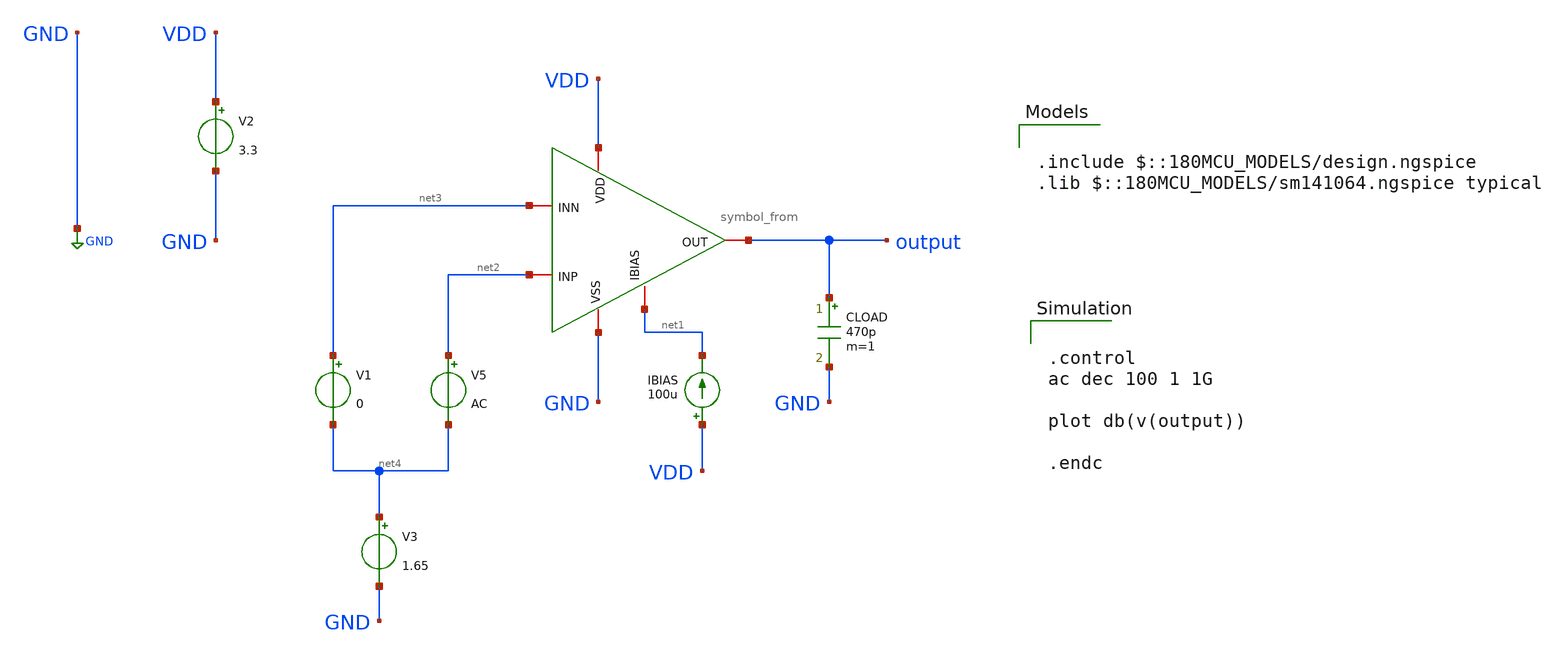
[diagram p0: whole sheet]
** sch_path: designs/libs/core_amps/ota_folded_cascode/folded_cascode_tb.sch
**.subckt folded_cascode_tb
x1 VDD output net3 net2 net1 GND symbol_from
IBIAS VDD net1 100u
V2 VDD GND 3.3
CLOAD output GND 470p m=1
V1 net3 net4 0
V5 net2 net4 AC
V3 net4 GND 1.65
**** begin user architecture code

.include $::180MCU_MODELS/design.ngspice
.lib $::180MCU_MODELS/sm141064.ngspice typical



.control
ac dec 100 1 1G

plot db(v(output))

.endc


**** end user architecture code
**.ends

* expanding   symbol:  libs/core_amps/ota_folded_cascode/symbol_from.sym # of pins=6
** sym_path: designs/libs/core_amps/ota_folded_cascode/symbol_from.sym
** sch_path: designs/libs/core_amps/ota_folded_cascode/symbol_from.sch
.subckt symbol_from VDD OUT INN INP IBIAS VSS
*.iopin IBIAS
*.iopin INN
*.iopin INP
*.iopin OUT
*.iopin VSS
*.iopin VDD
XM1 IBIAS IBIAS VSS VSS nfet_03v3 L=.5u W=23u nf=1 ad='int((nf+1)/2) * W/nf * 0.18u' as='int((nf+2)/2) * W/nf * 0.18u'
+ pd='2*int((nf+1)/2) * (W/nf + 0.18u)' ps='2*int((nf+2)/2) * (W/nf + 0.18u)' nrd='0.18u / W' nrs='0.18u / W'
+ sa=0 sb=0 sd=0 m=1
XM2 net2 net9 VDD VDD pfet_03v3 L=.5u W=100u nf=1 ad='int((nf+1)/2) * W/nf * 0.18u' as='int((nf+2)/2) * W/nf * 0.18u'
+ pd='2*int((nf+1)/2) * (W/nf + 0.18u)' ps='2*int((nf+2)/2) * (W/nf + 0.18u)' nrd='0.18u / W' nrs='0.18u / W'
+ sa=0 sb=0 sd=0 m=1.5
XM3 OUT net3 net2 VDD pfet_03v3 L=0.5u W=78u nf=1 ad='int((nf+1)/2) * W/nf * 0.18u' as='int((nf+2)/2) * W/nf * 0.18u'
+ pd='2*int((nf+1)/2) * (W/nf + 0.18u)' ps='2*int((nf+2)/2) * (W/nf + 0.18u)' nrd='0.18u / W' nrs='0.18u / W'
+ sa=0 sb=0 sd=0 m=1
XM4 net4 net3 net1 VDD pfet_03v3 L=0.5u W=78u nf=1 ad='int((nf+1)/2) * W/nf * 0.18u' as='int((nf+2)/2) * W/nf * 0.18u'
+ pd='2*int((nf+1)/2) * (W/nf + 0.18u)' ps='2*int((nf+2)/2) * (W/nf + 0.18u)' nrd='0.18u / W' nrs='0.18u / W'
+ sa=0 sb=0 sd=0 m=1
XM5 net1 net9 VDD VDD pfet_03v3 L=.5u W=100u nf=1 ad='int((nf+1)/2) * W/nf * 0.18u' as='int((nf+2)/2) * W/nf * 0.18u'
+ pd='2*int((nf+1)/2) * (W/nf + 0.18u)' ps='2*int((nf+2)/2) * (W/nf + 0.18u)' nrd='0.18u / W' nrs='0.18u / W'
+ sa=0 sb=0 sd=0 m=1.5
XM6 net4 net5 net7 VSS nfet_03v3 L=0.5u W=23u nf=1 ad='int((nf+1)/2) * W/nf * 0.18u' as='int((nf+2)/2) * W/nf * 0.18u'
+ pd='2*int((nf+1)/2) * (W/nf + 0.18u)' ps='2*int((nf+2)/2) * (W/nf + 0.18u)' nrd='0.18u / W' nrs='0.18u / W'
+ sa=0 sb=0 sd=0 m=1
XM7 OUT net5 net6 VSS nfet_03v3 L=0.5u W=23u nf=1 ad='int((nf+1)/2) * W/nf * 0.18u' as='int((nf+2)/2) * W/nf * 0.18u'
+ pd='2*int((nf+1)/2) * (W/nf + 0.18u)' ps='2*int((nf+2)/2) * (W/nf + 0.18u)' nrd='0.18u / W' nrs='0.18u / W'
+ sa=0 sb=0 sd=0 m=1
XM8 net7 net4 VSS VSS nfet_03v3 L=.5u W=23u nf=1 ad='int((nf+1)/2) * W/nf * 0.18u' as='int((nf+2)/2) * W/nf * 0.18u'
+ pd='2*int((nf+1)/2) * (W/nf + 0.18u)' ps='2*int((nf+2)/2) * (W/nf + 0.18u)' nrd='0.18u / W' nrs='0.18u / W'
+ sa=0 sb=0 sd=0 m=2
XM9 net6 net4 VSS VSS nfet_03v3 L=.5u W=23u nf=1 ad='int((nf+1)/2) * W/nf * 0.18u' as='int((nf+2)/2) * W/nf * 0.18u'
+ pd='2*int((nf+1)/2) * (W/nf + 0.18u)' ps='2*int((nf+2)/2) * (W/nf + 0.18u)' nrd='0.18u / W' nrs='0.18u / W'
+ sa=0 sb=0 sd=0 m=2
XM10 net1 INP net8 VSS nfet_03v3 L=.5u W=11.5u nf=1 ad='int((nf+1)/2) * W/nf * 0.18u' as='int((nf+2)/2) * W/nf * 0.18u'
+ pd='2*int((nf+1)/2) * (W/nf + 0.18u)' ps='2*int((nf+2)/2) * (W/nf + 0.18u)' nrd='0.18u / W' nrs='0.18u / W'
+ sa=0 sb=0 sd=0 m=1
XM12 net8 IBIAS VSS VSS nfet_03v3 L=.5u W=23u nf=1 ad='int((nf+1)/2) * W/nf * 0.18u' as='int((nf+2)/2) * W/nf * 0.18u'
+ pd='2*int((nf+1)/2) * (W/nf + 0.18u)' ps='2*int((nf+2)/2) * (W/nf + 0.18u)' nrd='0.18u / W' nrs='0.18u / W'
+ sa=0 sb=0 sd=0 m=1
XM18 net9 net9 VDD VDD pfet_03v3 L=.5u W=78u nf=1 ad='int((nf+1)/2) * W/nf * 0.18u' as='int((nf+2)/2) * W/nf * 0.18u'
+ pd='2*int((nf+1)/2) * (W/nf + 0.18u)' ps='2*int((nf+2)/2) * (W/nf + 0.18u)' nrd='0.18u / W' nrs='0.18u / W'
+ sa=0 sb=0 sd=0 m=1
XM11 net2 INN net8 VSS nfet_03v3 L=.5u W=11.5u nf=1 ad='int((nf+1)/2) * W/nf * 0.18u' as='int((nf+2)/2) * W/nf * 0.18u'
+ pd='2*int((nf+1)/2) * (W/nf + 0.18u)' ps='2*int((nf+2)/2) * (W/nf + 0.18u)' nrd='0.18u / W' nrs='0.18u / W'
+ sa=0 sb=0 sd=0 m=1
XM13 net9 IBIAS VSS VSS nfet_03v3 L=.5u W=23u nf=1 ad='int((nf+1)/2) * W/nf * 0.18u' as='int((nf+2)/2) * W/nf * 0.18u'
+ pd='2*int((nf+1)/2) * (W/nf + 0.18u)' ps='2*int((nf+2)/2) * (W/nf + 0.18u)' nrd='0.18u / W' nrs='0.18u / W'
+ sa=0 sb=0 sd=0 m=1
V5 net3 VSS 2.0
V1 net5 VSS 1.2
.ends

.GLOBAL GND
.end
